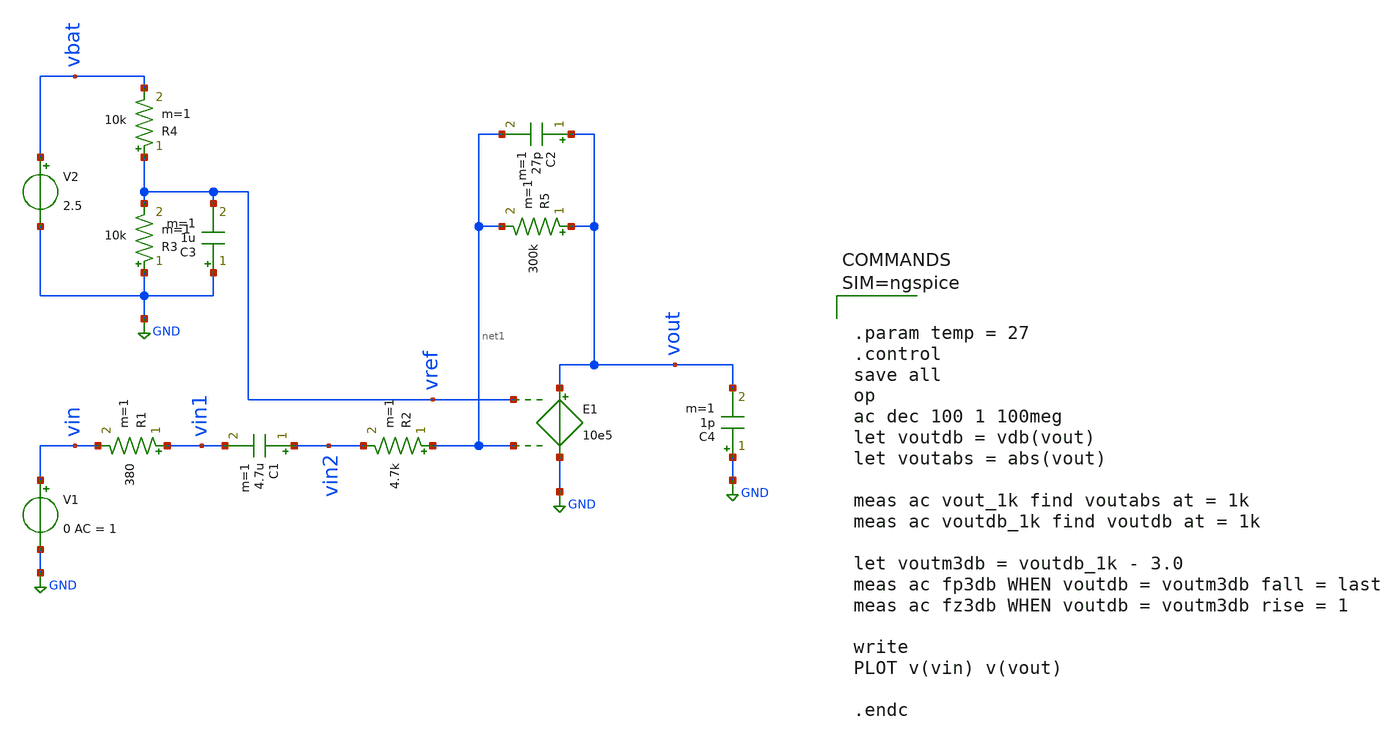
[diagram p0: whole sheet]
** sch_path: sch/MEMS_mic.sch
**.subckt MEMS_mic
V1 vin GND 0 AC = 1
C1 vin2 vin1 4.7u m=1
R1 vin1 vin 380 m=1
R2 net1 vin2 4.7k m=1
R3 GND vref 10k m=1
R4 vref vbat 10k m=1
C3 GND vref 1u m=1
C4 GND vout 1p m=1
V2 vbat GND 2.5
R5 vout net1 300k m=1
C2 vout net1 27p m=1
E1 vout GND vref net1 10e5
**** begin user architecture code



.param temp = 27
.control
save all
op
ac dec 100 1 100meg
let voutdb = vdb(vout)
let voutabs = abs(vout)

meas ac vout_1k find voutabs at = 1k
meas ac voutdb_1k find voutdb at = 1k

let voutm3db = voutdb_1k - 3.0
meas ac fp3db WHEN voutdb = voutm3db fall = last
meas ac fz3db WHEN voutdb = voutm3db rise = 1

write
PLOT v(vin) v(vout)

.endc



**** end user architecture code
**.ends
.GLOBAL GND
.end
